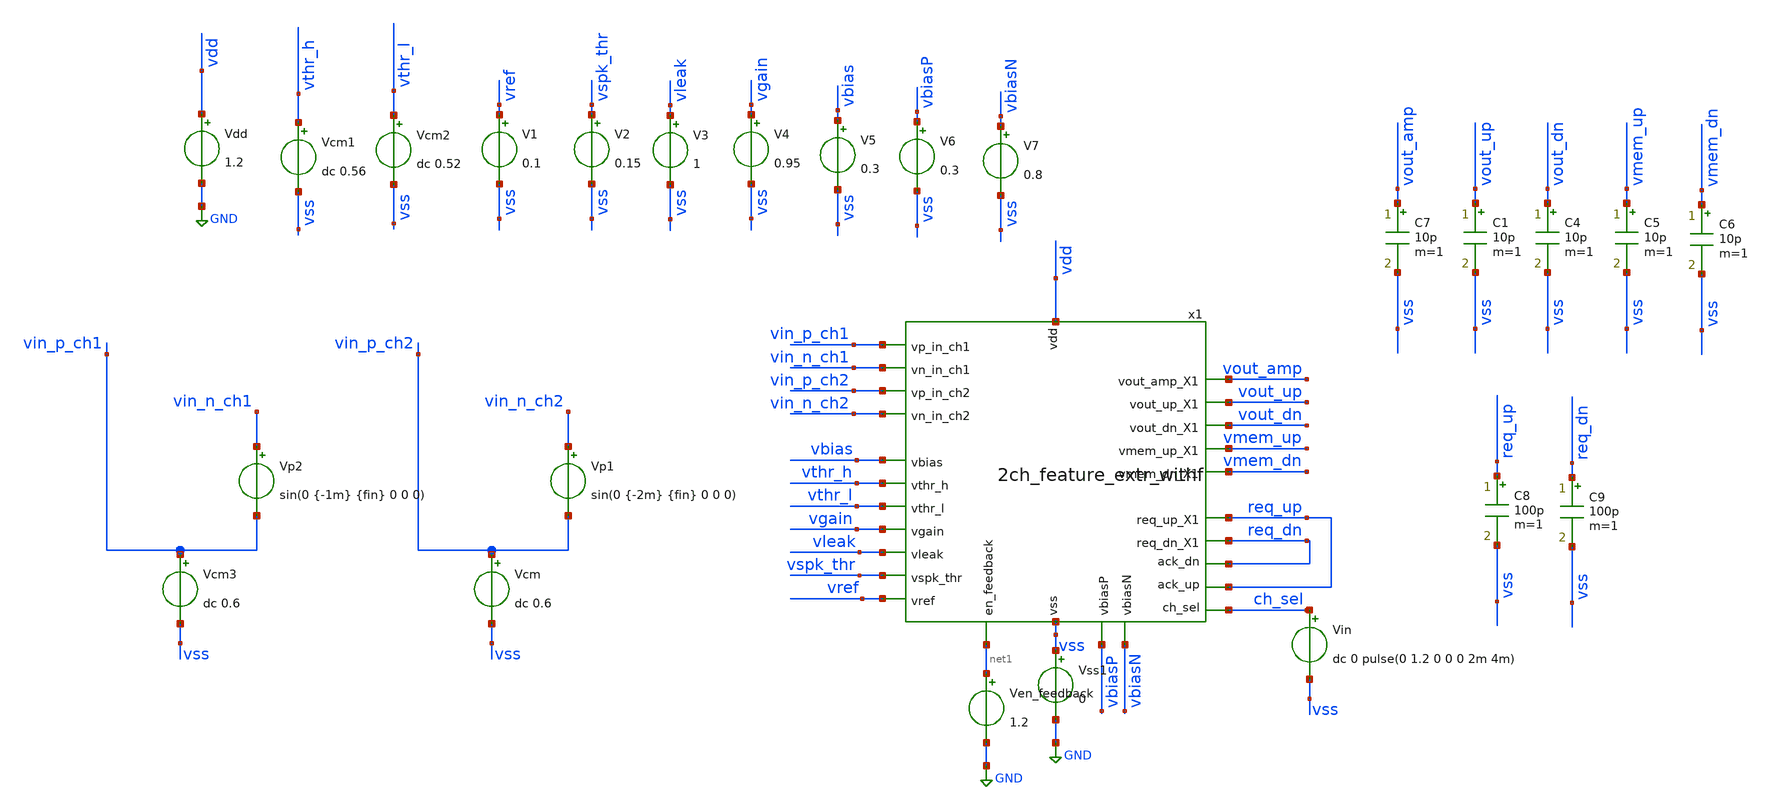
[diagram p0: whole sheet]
** sch_path: v2_feature_extr_withf/2ch_feature_extr_tb.sch
**.subckt 2ch_feature_extr_tb
x1 net1 vbias vdd vbiasP vss vbiasN vgain vleak vspk_thr vref vthr_h vin_p_ch1 req_up req_dn
+ vin_n_ch1 vthr_l ch_sel vout_up vmem_dn vmem_up vout_dn vin_p_ch2 vin_n_ch2 vout_amp req_up req_dn
+ 2ch_feature_extr_withf
Vdd vdd GND 1.2
Vcm1 vthr_h vss dc 0.56
Vcm2 vthr_l vss dc 0.52
V1 vref vss 0.1
V2 vspk_thr vss 0.15
V3 vleak vss 1
V4 vgain vss 0.95
Vcm vin_p_ch2 vss dc 0.6
Vp1 vin_n_ch2 vin_p_ch2 sin(0 {-2m} {fin} 0 0 0)
V5 vbias vss 0.3
Vss1 vss GND 0
Vcm3 vin_p_ch1 vss dc 0.6
Vp2 vin_n_ch1 vin_p_ch1 sin(0 {-1m} {fin} 0 0 0)
Vin ch_sel vss dc 0 pulse(0 1.2 0 0 0 2m 4m)
V6 vbiasP vss 0.3
V7 vbiasN vss 0.8
C7 vout_amp vss 10p m=1
C1 vout_up vss 10p m=1
C4 vout_dn vss 10p m=1
C5 vmem_up vss 10p m=1
C6 vmem_dn vss 10p m=1
C8 req_up vss 100p m=1
C9 req_dn vss 100p m=1
Ven_feedback net1 GND 1.2
**** begin user architecture code


.temp 27
.param fin=1K
*.param amp=1m
.control
.options gmin=1e-17 rshunt=1e12 reltol=1e-3 abstol=1e-9 vntol=1e-6

option sparse
save all

op
write 2ch_feature_extr_tb.raw
set appendwrite

tran 100n 2m
write 2ch_feature_extr_tb.raw

.endc



.lib cornerMOSlv.lib mos_tt
.lib cornerMOShv.lib mos_tt
.include $::PDK_ROOT/ihp-sg13cmos5l/libs.ref/sg13cmos5l_stdcell/spice/sg13cmos5l_stdcell.spice
.include $::PDK_ROOT/ihp-sg13cmos5l/libs.tech/ngspice/models/cap_mfringe.lib

**** end user architecture code
**.ends
.GLOBAL GND
.end
